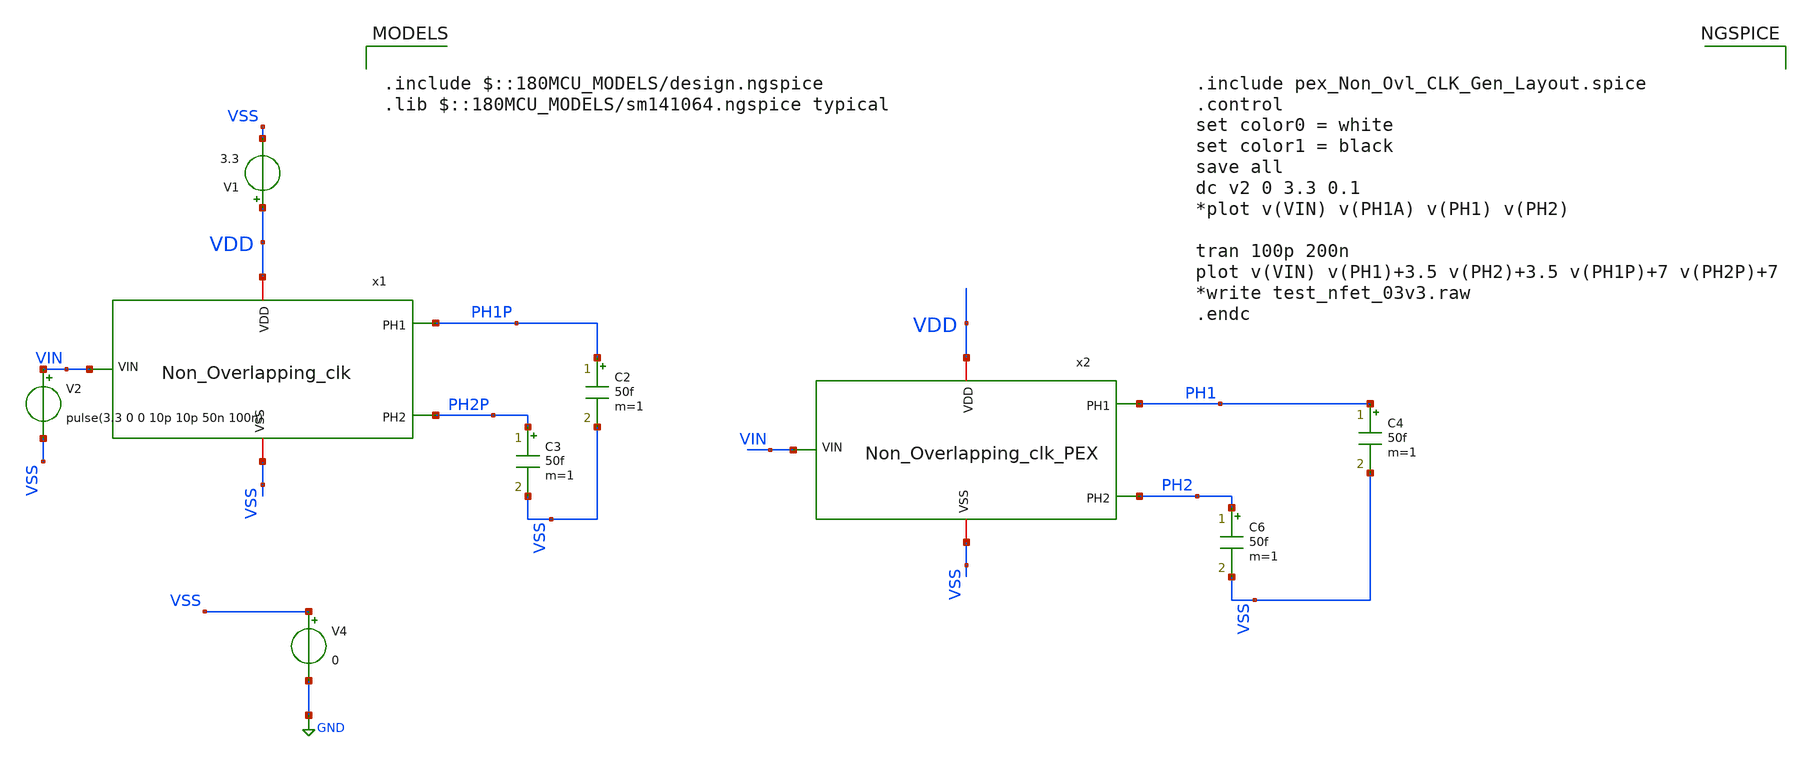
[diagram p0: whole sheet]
** sch_path: SCOP_INPUT_AND_MUX_PAKISTAN_03/Xschem/Non_OvL_CLK_Gen/Non_Overlapping_Clk_TB.sch
**.subckt Non_Overlapping_Clk_TB
C2 PH1P VSS 50f m=1
C3 PH2P VSS 50f m=1
V1 VDD VSS 3.3
V2 VIN VSS pulse(3.3 0 0 10p 10p 50n 100n)
V4 VSS GND 0
x1 VSS VDD VIN PH1P PH2P Non_Overlapping_clk
C4 PH1 VSS 50f m=1
C6 PH2 VSS 50f m=1
x2 VSS VDD VIN PH1 PH2 Non_Overlapping_clk_PEX
**** begin user architecture code

.include $::180MCU_MODELS/design.ngspice
.lib $::180MCU_MODELS/sm141064.ngspice typical



.include pex_Non_Ovl_CLK_Gen_Layout.spice
.control
set color0 = white
set color1 = black
save all
dc v2 0 3.3 0.1
*plot v(VIN) v(PH1A) v(PH1) v(PH2)

tran 100p 200n
plot v(VIN) v(PH1)+3.5 v(PH2)+3.5 v(PH1P)+7 v(PH2P)+7
*write test_nfet_03v3.raw
.endc


**** end user architecture code
**.ends
.GLOBAL GND
.end
